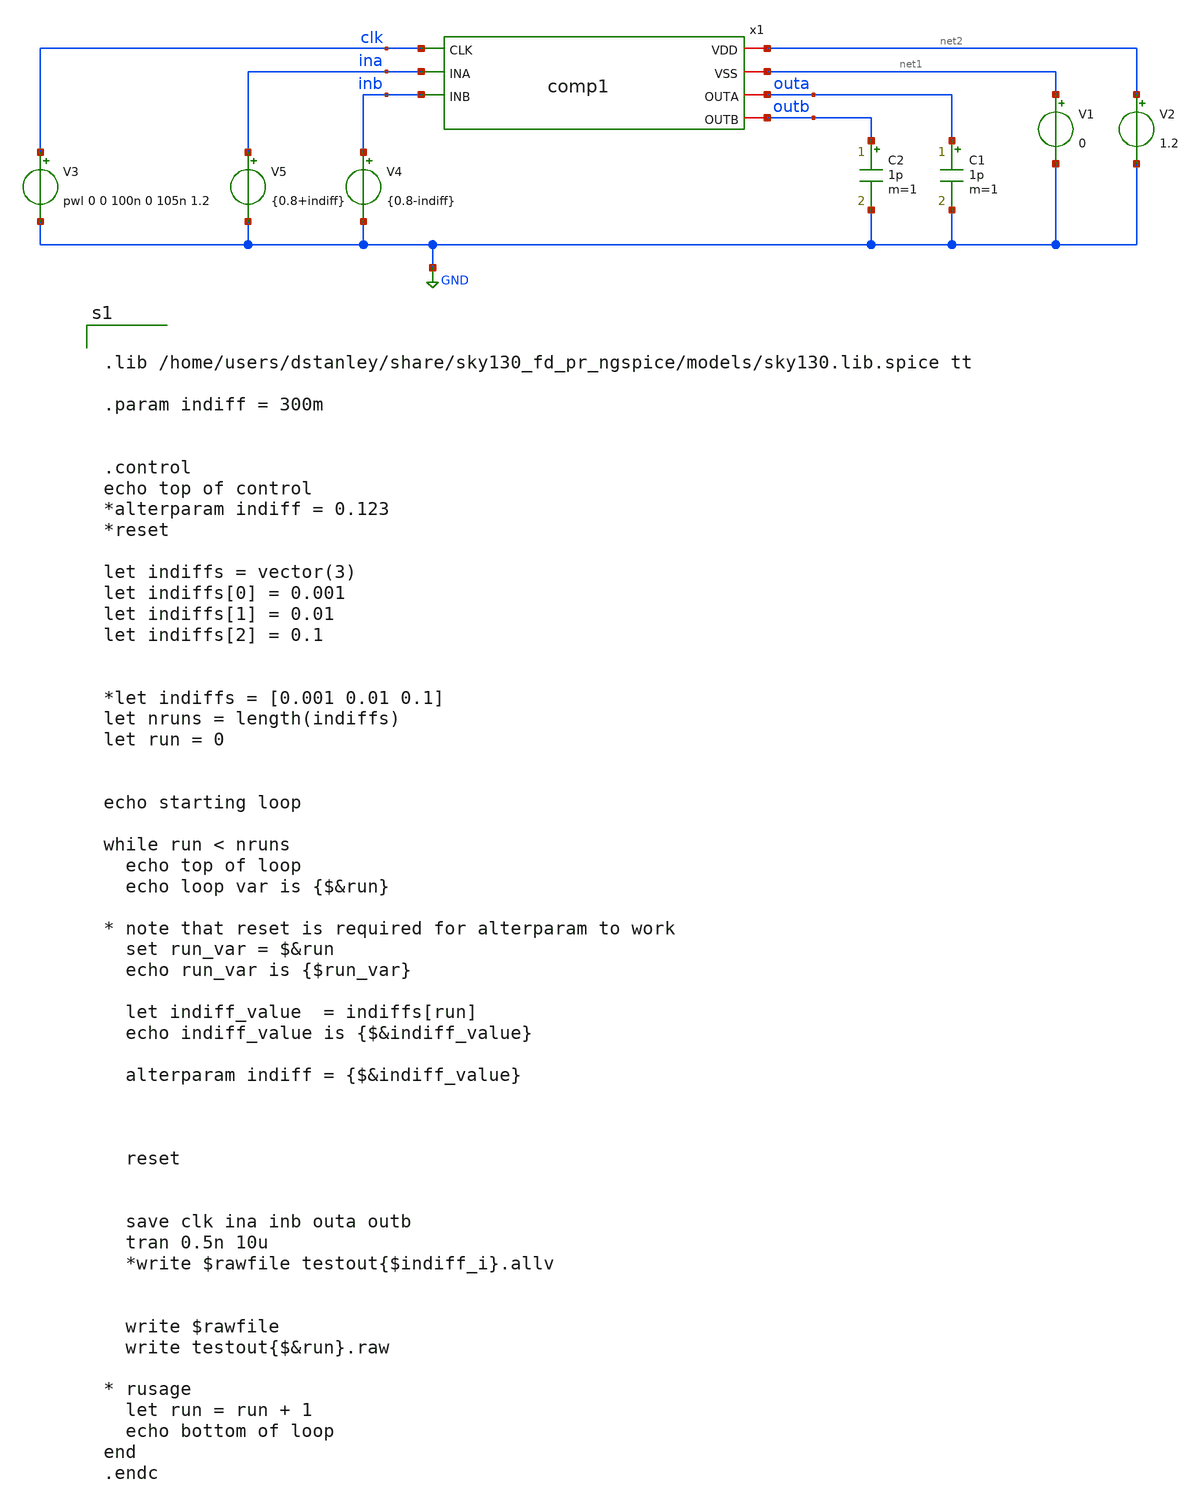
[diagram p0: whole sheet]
** sch_path: backup_comp1.sch
**.subckt backup_comp1
x1 net2 net1 clk ina inb outa outb comp1
V1 net1 GND 0
V2 net2 GND 1.2
C1 outa GND 1p m=1
C2 outb GND 1p m=1
V3 clk GND pwl 0 0 100n 0 105n 1.2
V4 inb GND {0.8-indiff}
V5 ina GND {0.8+indiff}
**** begin user architecture code


.lib /home/users/dstanley/share/sky130_fd_pr_ngspice/models/sky130.lib.spice tt

.param indiff = 300m


.control
echo top of control
*alterparam indiff = 0.123
*reset

let indiffs = vector(3)
let indiffs[0] = 0.001
let indiffs[1] = 0.01
let indiffs[2] = 0.1


*let indiffs = [0.001 0.01 0.1]
let nruns = length(indiffs)
let run = 0


echo starting loop

while run < nruns
  echo top of loop
  echo loop var is {$&run}

* note that reset is required for alterparam to work
  set run_var = $&run
  echo run_var is {$run_var}

  let indiff_value  = indiffs[run]
  echo indiff_value is {$&indiff_value}

  alterparam indiff = {$&indiff_value}



  reset


  save clk ina inb outa outb
  tran 0.5n 10u
  *write $rawfile testout{$indiff_i}.allv


  write $rawfile
  write testout{$&run}.raw

* rusage
  let run = run + 1
  echo bottom of loop
end
.endc


**** end user architecture code
**.ends

* expanding   symbol:  /home/users/dstanley/EE272B/xschem_tests/comp1.sym # of pins=7
** sym_path: comp1.sym
** sch_path: comp1.sch
.subckt comp1 VDD VSS CLK INA INB OUTA OUTB
*.iopin VSS
*.iopin VDD
*.iopin OUTB
*.iopin OUTA
*.ipin INB
*.ipin INA
*.ipin CLK
XM1 net2 CLK VSS VSS sky130_fd_pr__nfet_01v8 L=0.15 W=1 nf=1 ad='int((nf+1)/2) * W/nf * 0.29' as='int((nf+2)/2) * W/nf * 0.29'
+ pd='2*int((nf+1)/2) * (W/nf + 0.29)' ps='2*int((nf+2)/2) * (W/nf + 0.29)' nrd='0.29 / W' nrs='0.29 / W'
+ sa=0 sb=0 sd=0 mult=1 m=1
XM2 net1 INA net2 VSS sky130_fd_pr__nfet_01v8 L=0.15 W=1 nf=1 ad='int((nf+1)/2) * W/nf * 0.29' as='int((nf+2)/2) * W/nf * 0.29'
+ pd='2*int((nf+1)/2) * (W/nf + 0.29)' ps='2*int((nf+2)/2) * (W/nf + 0.29)' nrd='0.29 / W' nrs='0.29 / W'
+ sa=0 sb=0 sd=0 mult=1 m=1
XM4 OUTB OUTA net1 VSS sky130_fd_pr__nfet_01v8 L=0.15 W=1 nf=1 ad='int((nf+1)/2) * W/nf * 0.29' as='int((nf+2)/2) * W/nf * 0.29'
+ pd='2*int((nf+1)/2) * (W/nf + 0.29)' ps='2*int((nf+2)/2) * (W/nf + 0.29)' nrd='0.29 / W' nrs='0.29 / W'
+ sa=0 sb=0 sd=0 mult=1 m=1
XM5 OUTB OUTA VDD VDD sky130_fd_pr__pfet_01v8 L=0.15 W=1 nf=1 ad='int((nf+1)/2) * W/nf * 0.29' as='int((nf+2)/2) * W/nf * 0.29'
+ pd='2*int((nf+1)/2) * (W/nf + 0.29)' ps='2*int((nf+2)/2) * (W/nf + 0.29)' nrd='0.29 / W' nrs='0.29 / W'
+ sa=0 sb=0 sd=0 mult=1 m=1
XM6 OUTB CLK VDD VDD sky130_fd_pr__pfet_01v8 L=0.15 W=1 nf=1 ad='int((nf+1)/2) * W/nf * 0.29' as='int((nf+2)/2) * W/nf * 0.29'
+ pd='2*int((nf+1)/2) * (W/nf + 0.29)' ps='2*int((nf+2)/2) * (W/nf + 0.29)' nrd='0.29 / W' nrs='0.29 / W'
+ sa=0 sb=0 sd=0 mult=1 m=1
XM3 net3 INB net2 VSS sky130_fd_pr__nfet_01v8 L=0.15 W=1 nf=1 ad='int((nf+1)/2) * W/nf * 0.29' as='int((nf+2)/2) * W/nf * 0.29'
+ pd='2*int((nf+1)/2) * (W/nf + 0.29)' ps='2*int((nf+2)/2) * (W/nf + 0.29)' nrd='0.29 / W' nrs='0.29 / W'
+ sa=0 sb=0 sd=0 mult=1 m=1
XM7 OUTA OUTB net3 VSS sky130_fd_pr__nfet_01v8 L=0.15 W=1 nf=1 ad='int((nf+1)/2) * W/nf * 0.29' as='int((nf+2)/2) * W/nf * 0.29'
+ pd='2*int((nf+1)/2) * (W/nf + 0.29)' ps='2*int((nf+2)/2) * (W/nf + 0.29)' nrd='0.29 / W' nrs='0.29 / W'
+ sa=0 sb=0 sd=0 mult=1 m=1
XM8 OUTA OUTB VDD VDD sky130_fd_pr__pfet_01v8 L=0.15 W=1 nf=1 ad='int((nf+1)/2) * W/nf * 0.29' as='int((nf+2)/2) * W/nf * 0.29'
+ pd='2*int((nf+1)/2) * (W/nf + 0.29)' ps='2*int((nf+2)/2) * (W/nf + 0.29)' nrd='0.29 / W' nrs='0.29 / W'
+ sa=0 sb=0 sd=0 mult=1 m=1
XM9 OUTA CLK VDD VDD sky130_fd_pr__pfet_01v8 L=0.15 W=1 nf=1 ad='int((nf+1)/2) * W/nf * 0.29' as='int((nf+2)/2) * W/nf * 0.29'
+ pd='2*int((nf+1)/2) * (W/nf + 0.29)' ps='2*int((nf+2)/2) * (W/nf + 0.29)' nrd='0.29 / W' nrs='0.29 / W'
+ sa=0 sb=0 sd=0 mult=1 m=1
.ends

.GLOBAL GND
.end
